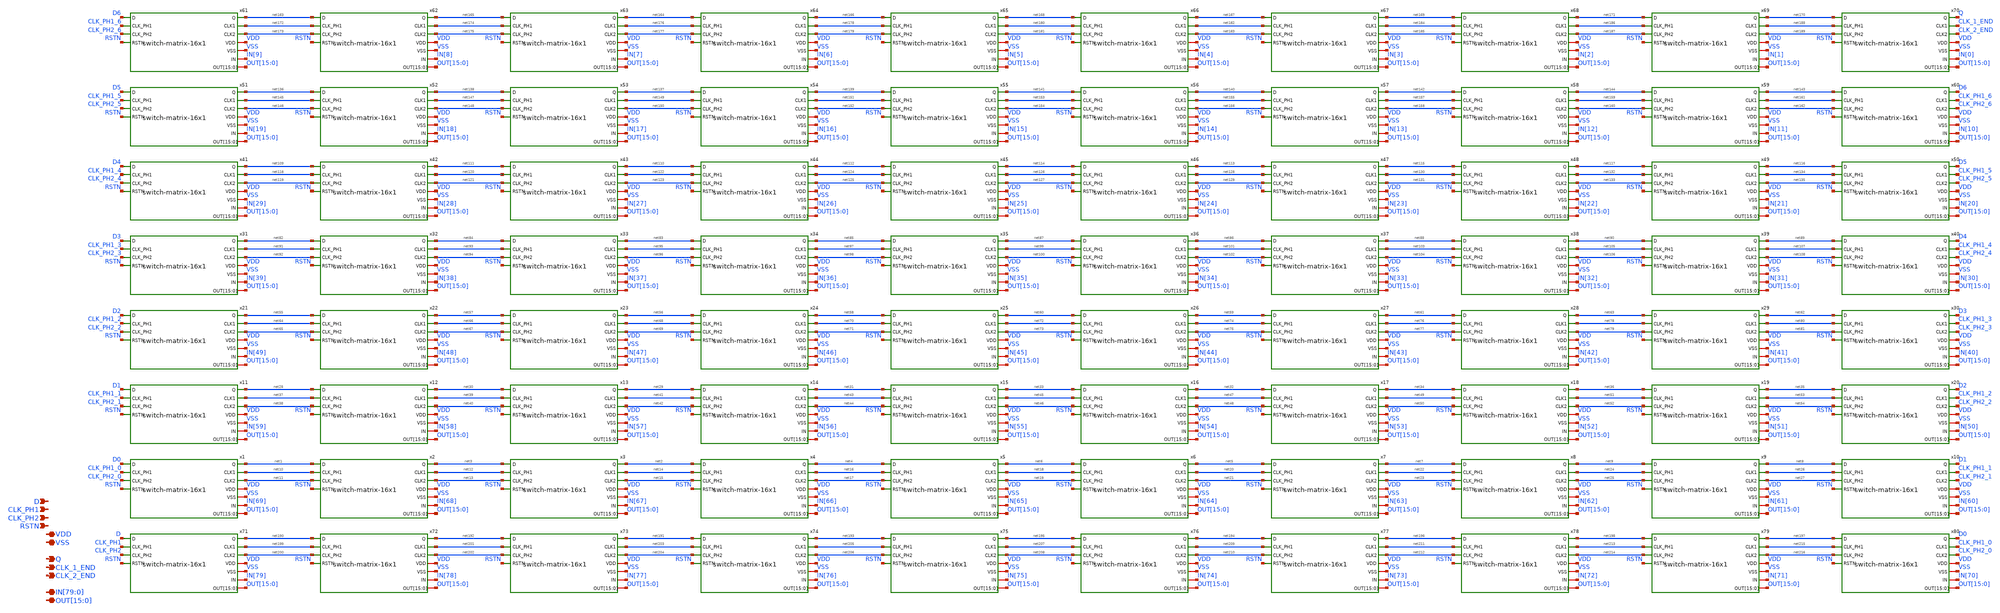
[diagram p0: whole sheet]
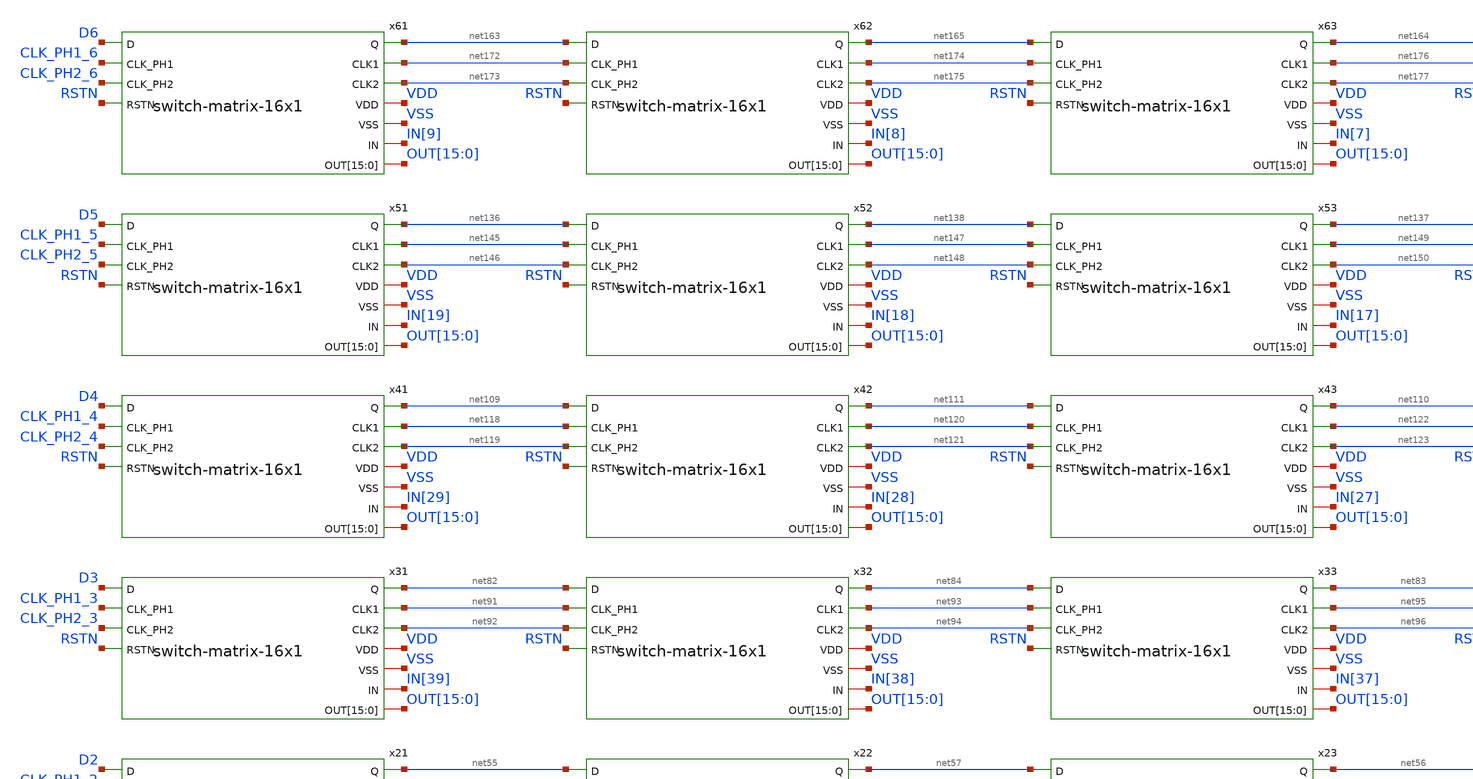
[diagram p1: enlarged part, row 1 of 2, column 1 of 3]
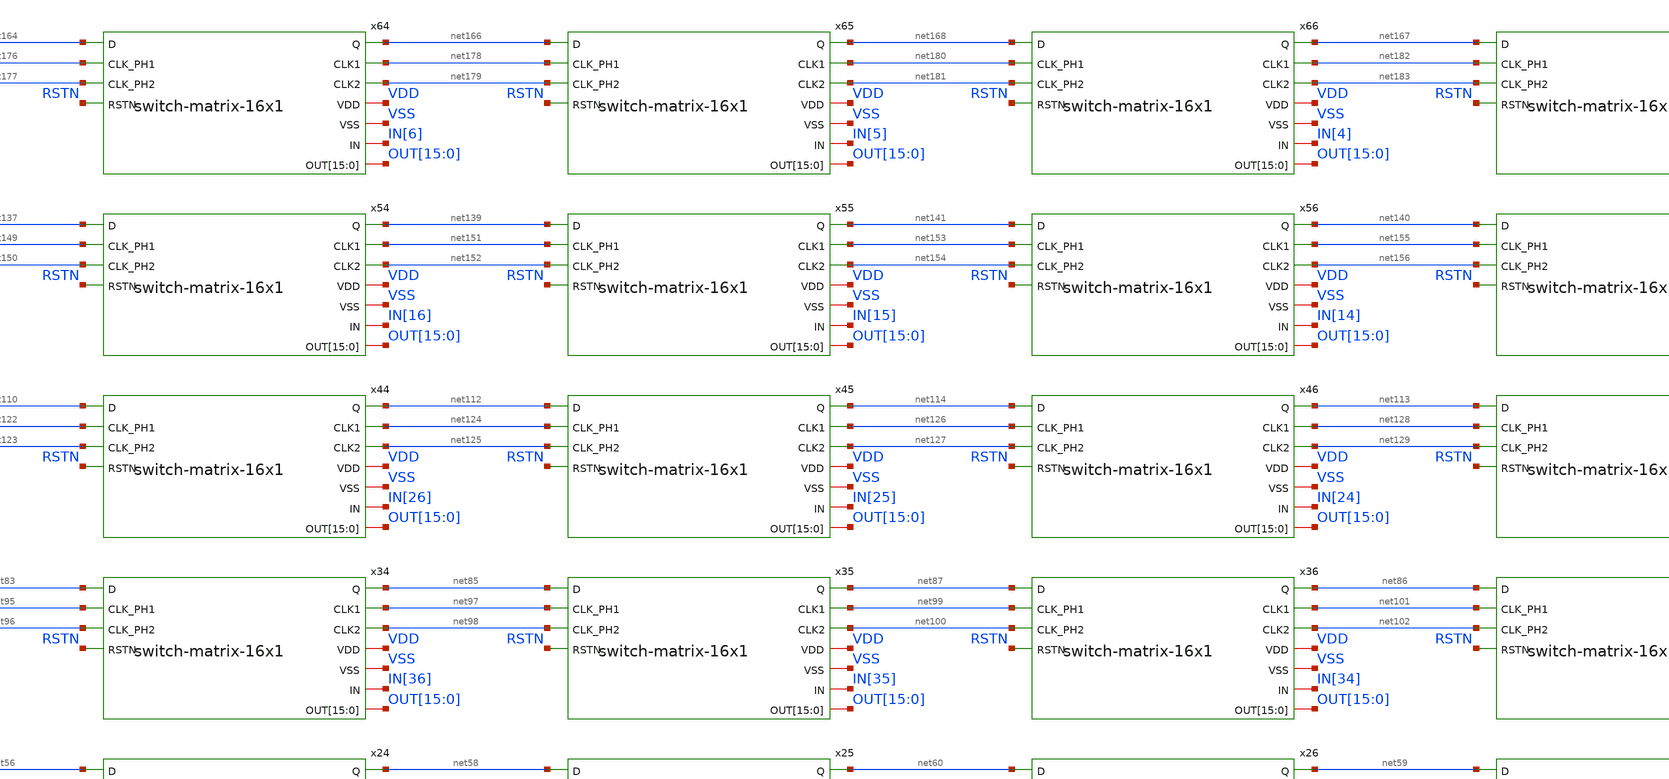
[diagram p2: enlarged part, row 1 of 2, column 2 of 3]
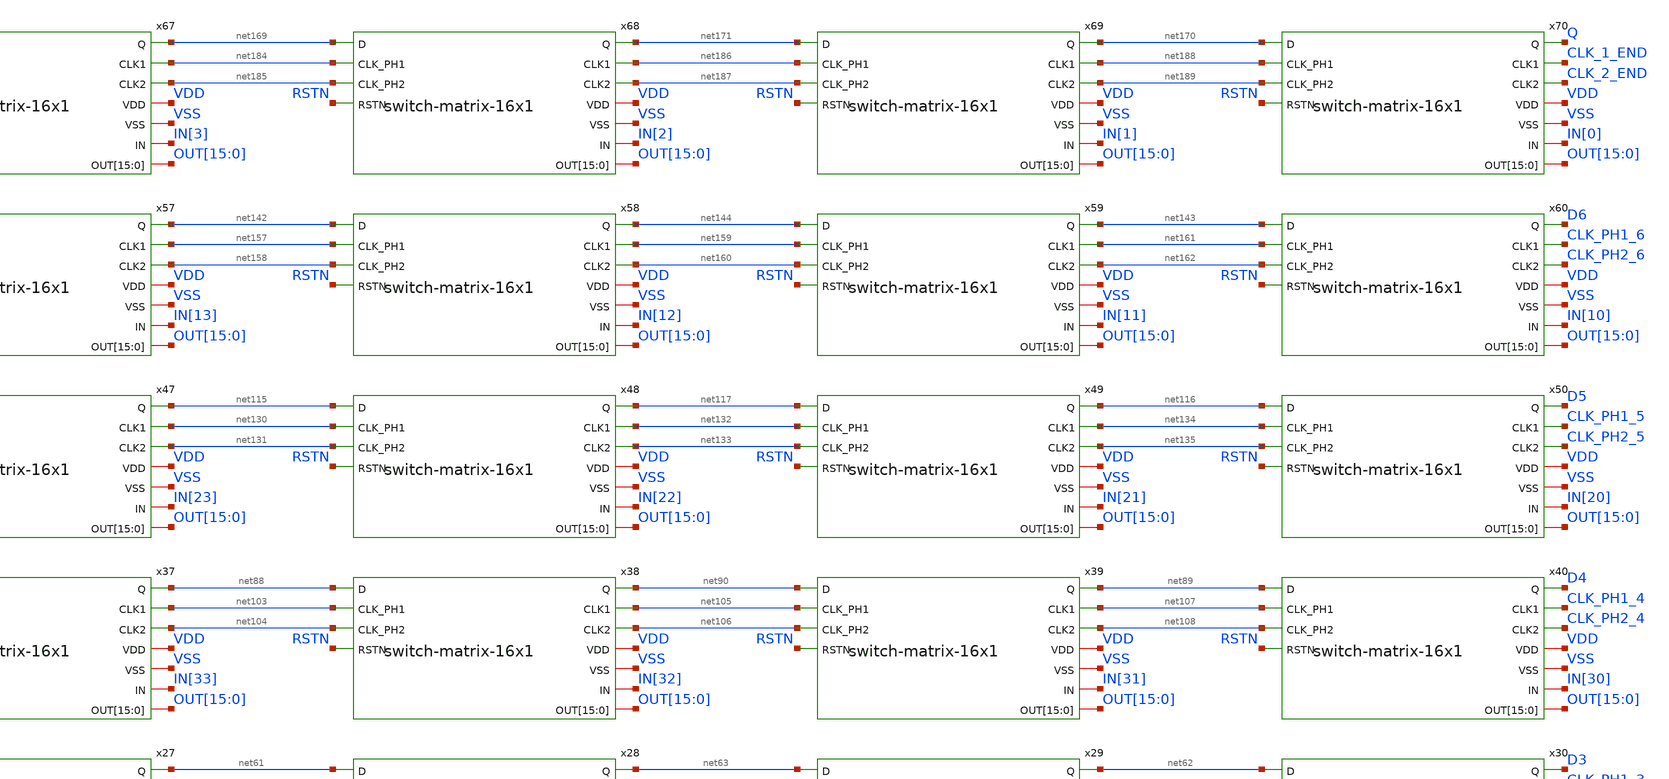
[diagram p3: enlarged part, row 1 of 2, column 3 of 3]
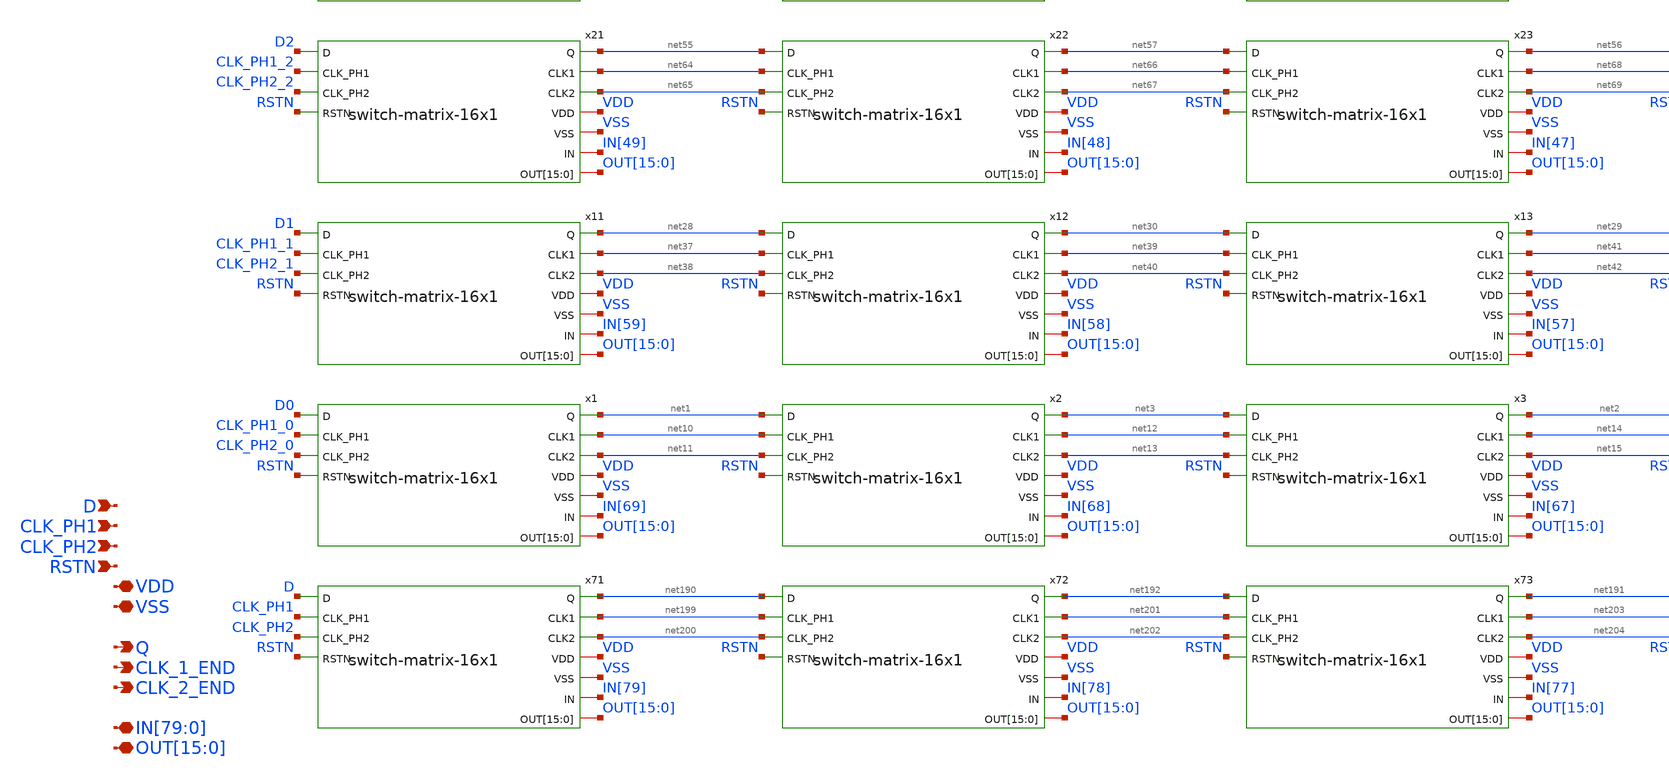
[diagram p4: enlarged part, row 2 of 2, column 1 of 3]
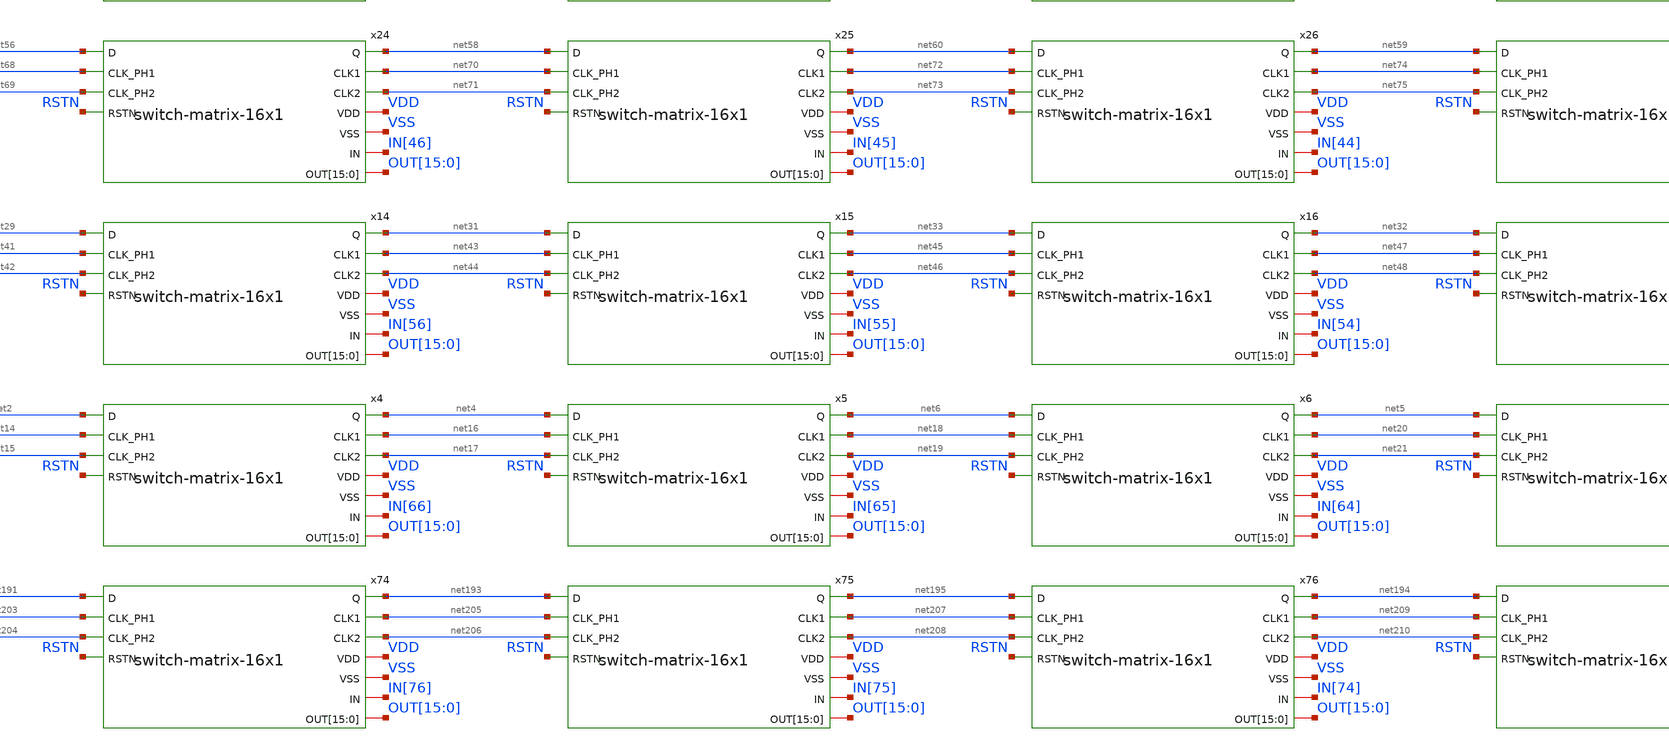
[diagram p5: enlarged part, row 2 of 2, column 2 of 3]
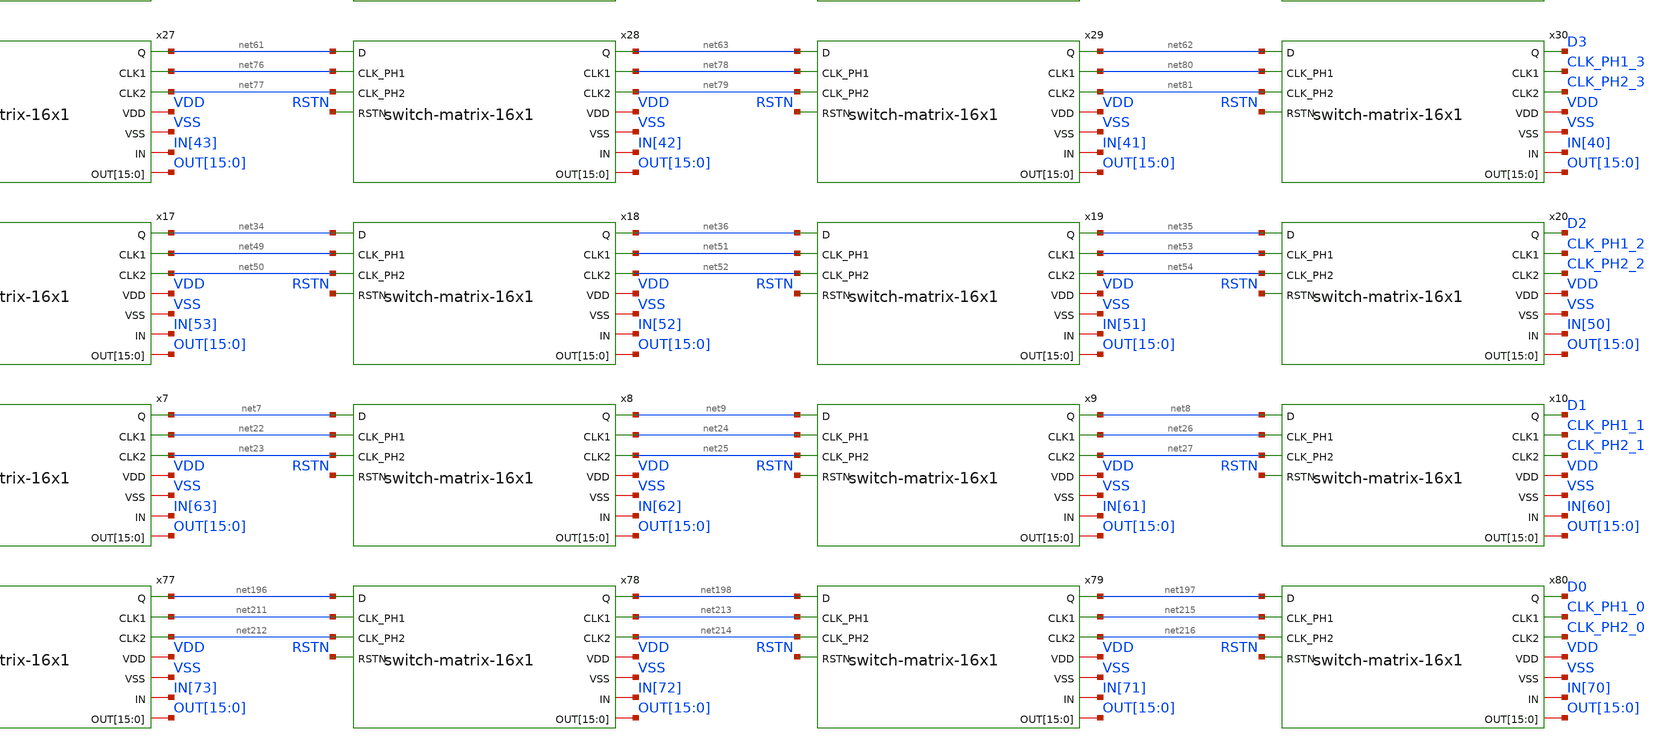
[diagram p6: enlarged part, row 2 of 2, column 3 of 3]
** sch_path: designs/libs/core_switch-matrix/switch-matrix-16x70/switch-matrix-16x70.sch
**.subckt switch-matrix-16x70 VDD VSS RSTN CLK_PH1 CLK_PH2 D
*+ IN[79],IN[78],IN[77],IN[76],IN[75],IN[74],IN[73],IN[72],IN[71],IN[70],IN[69],IN[68],IN[67],IN[66],IN[65],IN[64],IN[63],IN[62],IN[61],IN[60],IN[59],IN[58],IN[57],IN[56],IN[55],IN[54],IN[53],IN[52],IN[51],IN[50],IN[49],IN[48],IN[47],IN[46],IN[45],IN[44],IN[43],IN[42],IN[41],IN[40],IN[39],IN[38],IN[37],IN[36],IN[35],IN[34],IN[33],IN[32],IN[31],IN[30],IN[29],IN[28],IN[27],IN[26],IN[25],IN[24],IN[23],IN[22],IN[21],IN[20],IN[19],IN[18],IN[17],IN[16],IN[15],IN[14],IN[13],IN[12],IN[11],IN[10],IN[9],IN[8],IN[7],IN[6],IN[5],IN[4],IN[3],IN[2],IN[1],IN[0]
*+ OUT[15],OUT[14],OUT[13],OUT[12],OUT[11],OUT[10],OUT[9],OUT[8],OUT[7],OUT[6],OUT[5],OUT[4],OUT[3],OUT[2],OUT[1],OUT[0] Q CLK_1_END CLK_2_END
*.iopin VDD
*.iopin VSS
*.ipin RSTN
*.ipin CLK_PH1
*.ipin CLK_PH2
*.ipin D
*.iopin
*+ IN[79],IN[78],IN[77],IN[76],IN[75],IN[74],IN[73],IN[72],IN[71],IN[70],IN[69],IN[68],IN[67],IN[66],IN[65],IN[64],IN[63],IN[62],IN[61],IN[60],IN[59],IN[58],IN[57],IN[56],IN[55],IN[54],IN[53],IN[52],IN[51],IN[50],IN[49],IN[48],IN[47],IN[46],IN[45],IN[44],IN[43],IN[42],IN[41],IN[40],IN[39],IN[38],IN[37],IN[36],IN[35],IN[34],IN[33],IN[32],IN[31],IN[30],IN[29],IN[28],IN[27],IN[26],IN[25],IN[24],IN[23],IN[22],IN[21],IN[20],IN[19],IN[18],IN[17],IN[16],IN[15],IN[14],IN[13],IN[12],IN[11],IN[10],IN[9],IN[8],IN[7],IN[6],IN[5],IN[4],IN[3],IN[2],IN[1],IN[0]
*.iopin
*+ OUT[15],OUT[14],OUT[13],OUT[12],OUT[11],OUT[10],OUT[9],OUT[8],OUT[7],OUT[6],OUT[5],OUT[4],OUT[3],OUT[2],OUT[1],OUT[0]
*.opin Q
*.opin CLK_1_END
*.opin CLK_2_END
x1 net1 net10 net11 VDD VSS IN[69] OUT[15] OUT[14] OUT[13] OUT[12] OUT[11] OUT[10] OUT[9] OUT[8]
+ OUT[7] OUT[6] OUT[5] OUT[4] OUT[3] OUT[2] OUT[1] OUT[0] D0 CLK_PH1_0 CLK_PH2_0 RSTN switch-matrix-16x1
x2 net3 net12 net13 VDD VSS IN[68] OUT[15] OUT[14] OUT[13] OUT[12] OUT[11] OUT[10] OUT[9] OUT[8]
+ OUT[7] OUT[6] OUT[5] OUT[4] OUT[3] OUT[2] OUT[1] OUT[0] net1 net10 net11 RSTN switch-matrix-16x1
x3 net2 net14 net15 VDD VSS IN[67] OUT[15] OUT[14] OUT[13] OUT[12] OUT[11] OUT[10] OUT[9] OUT[8]
+ OUT[7] OUT[6] OUT[5] OUT[4] OUT[3] OUT[2] OUT[1] OUT[0] net3 net12 net13 RSTN switch-matrix-16x1
x4 net4 net16 net17 VDD VSS IN[66] OUT[15] OUT[14] OUT[13] OUT[12] OUT[11] OUT[10] OUT[9] OUT[8]
+ OUT[7] OUT[6] OUT[5] OUT[4] OUT[3] OUT[2] OUT[1] OUT[0] net2 net14 net15 RSTN switch-matrix-16x1
x5 net6 net18 net19 VDD VSS IN[65] OUT[15] OUT[14] OUT[13] OUT[12] OUT[11] OUT[10] OUT[9] OUT[8]
+ OUT[7] OUT[6] OUT[5] OUT[4] OUT[3] OUT[2] OUT[1] OUT[0] net4 net16 net17 RSTN switch-matrix-16x1
x6 net5 net20 net21 VDD VSS IN[64] OUT[15] OUT[14] OUT[13] OUT[12] OUT[11] OUT[10] OUT[9] OUT[8]
+ OUT[7] OUT[6] OUT[5] OUT[4] OUT[3] OUT[2] OUT[1] OUT[0] net6 net18 net19 RSTN switch-matrix-16x1
x7 net7 net22 net23 VDD VSS IN[63] OUT[15] OUT[14] OUT[13] OUT[12] OUT[11] OUT[10] OUT[9] OUT[8]
+ OUT[7] OUT[6] OUT[5] OUT[4] OUT[3] OUT[2] OUT[1] OUT[0] net5 net20 net21 RSTN switch-matrix-16x1
x8 net9 net24 net25 VDD VSS IN[62] OUT[15] OUT[14] OUT[13] OUT[12] OUT[11] OUT[10] OUT[9] OUT[8]
+ OUT[7] OUT[6] OUT[5] OUT[4] OUT[3] OUT[2] OUT[1] OUT[0] net7 net22 net23 RSTN switch-matrix-16x1
x9 net8 net26 net27 VDD VSS IN[61] OUT[15] OUT[14] OUT[13] OUT[12] OUT[11] OUT[10] OUT[9] OUT[8]
+ OUT[7] OUT[6] OUT[5] OUT[4] OUT[3] OUT[2] OUT[1] OUT[0] net9 net24 net25 RSTN switch-matrix-16x1
x10 D1 CLK_PH1_1 CLK_PH2_1 VDD VSS IN[60] OUT[15] OUT[14] OUT[13] OUT[12] OUT[11] OUT[10] OUT[9]
+ OUT[8] OUT[7] OUT[6] OUT[5] OUT[4] OUT[3] OUT[2] OUT[1] OUT[0] net8 net26 net27 RSTN switch-matrix-16x1
x11 net28 net37 net38 VDD VSS IN[59] OUT[15] OUT[14] OUT[13] OUT[12] OUT[11] OUT[10] OUT[9] OUT[8]
+ OUT[7] OUT[6] OUT[5] OUT[4] OUT[3] OUT[2] OUT[1] OUT[0] D1 CLK_PH1_1 CLK_PH2_1 RSTN switch-matrix-16x1
x12 net30 net39 net40 VDD VSS IN[58] OUT[15] OUT[14] OUT[13] OUT[12] OUT[11] OUT[10] OUT[9] OUT[8]
+ OUT[7] OUT[6] OUT[5] OUT[4] OUT[3] OUT[2] OUT[1] OUT[0] net28 net37 net38 RSTN switch-matrix-16x1
x13 net29 net41 net42 VDD VSS IN[57] OUT[15] OUT[14] OUT[13] OUT[12] OUT[11] OUT[10] OUT[9] OUT[8]
+ OUT[7] OUT[6] OUT[5] OUT[4] OUT[3] OUT[2] OUT[1] OUT[0] net30 net39 net40 RSTN switch-matrix-16x1
x14 net31 net43 net44 VDD VSS IN[56] OUT[15] OUT[14] OUT[13] OUT[12] OUT[11] OUT[10] OUT[9] OUT[8]
+ OUT[7] OUT[6] OUT[5] OUT[4] OUT[3] OUT[2] OUT[1] OUT[0] net29 net41 net42 RSTN switch-matrix-16x1
x15 net33 net45 net46 VDD VSS IN[55] OUT[15] OUT[14] OUT[13] OUT[12] OUT[11] OUT[10] OUT[9] OUT[8]
+ OUT[7] OUT[6] OUT[5] OUT[4] OUT[3] OUT[2] OUT[1] OUT[0] net31 net43 net44 RSTN switch-matrix-16x1
x16 net32 net47 net48 VDD VSS IN[54] OUT[15] OUT[14] OUT[13] OUT[12] OUT[11] OUT[10] OUT[9] OUT[8]
+ OUT[7] OUT[6] OUT[5] OUT[4] OUT[3] OUT[2] OUT[1] OUT[0] net33 net45 net46 RSTN switch-matrix-16x1
x17 net34 net49 net50 VDD VSS IN[53] OUT[15] OUT[14] OUT[13] OUT[12] OUT[11] OUT[10] OUT[9] OUT[8]
+ OUT[7] OUT[6] OUT[5] OUT[4] OUT[3] OUT[2] OUT[1] OUT[0] net32 net47 net48 RSTN switch-matrix-16x1
x18 net36 net51 net52 VDD VSS IN[52] OUT[15] OUT[14] OUT[13] OUT[12] OUT[11] OUT[10] OUT[9] OUT[8]
+ OUT[7] OUT[6] OUT[5] OUT[4] OUT[3] OUT[2] OUT[1] OUT[0] net34 net49 net50 RSTN switch-matrix-16x1
x19 net35 net53 net54 VDD VSS IN[51] OUT[15] OUT[14] OUT[13] OUT[12] OUT[11] OUT[10] OUT[9] OUT[8]
+ OUT[7] OUT[6] OUT[5] OUT[4] OUT[3] OUT[2] OUT[1] OUT[0] net36 net51 net52 RSTN switch-matrix-16x1
x20 D2 CLK_PH1_2 CLK_PH2_2 VDD VSS IN[50] OUT[15] OUT[14] OUT[13] OUT[12] OUT[11] OUT[10] OUT[9]
+ OUT[8] OUT[7] OUT[6] OUT[5] OUT[4] OUT[3] OUT[2] OUT[1] OUT[0] net35 net53 net54 RSTN switch-matrix-16x1
x21 net55 net64 net65 VDD VSS IN[49] OUT[15] OUT[14] OUT[13] OUT[12] OUT[11] OUT[10] OUT[9] OUT[8]
+ OUT[7] OUT[6] OUT[5] OUT[4] OUT[3] OUT[2] OUT[1] OUT[0] D2 CLK_PH1_2 CLK_PH2_2 RSTN switch-matrix-16x1
x22 net57 net66 net67 VDD VSS IN[48] OUT[15] OUT[14] OUT[13] OUT[12] OUT[11] OUT[10] OUT[9] OUT[8]
+ OUT[7] OUT[6] OUT[5] OUT[4] OUT[3] OUT[2] OUT[1] OUT[0] net55 net64 net65 RSTN switch-matrix-16x1
x23 net56 net68 net69 VDD VSS IN[47] OUT[15] OUT[14] OUT[13] OUT[12] OUT[11] OUT[10] OUT[9] OUT[8]
+ OUT[7] OUT[6] OUT[5] OUT[4] OUT[3] OUT[2] OUT[1] OUT[0] net57 net66 net67 RSTN switch-matrix-16x1
x24 net58 net70 net71 VDD VSS IN[46] OUT[15] OUT[14] OUT[13] OUT[12] OUT[11] OUT[10] OUT[9] OUT[8]
+ OUT[7] OUT[6] OUT[5] OUT[4] OUT[3] OUT[2] OUT[1] OUT[0] net56 net68 net69 RSTN switch-matrix-16x1
x25 net60 net72 net73 VDD VSS IN[45] OUT[15] OUT[14] OUT[13] OUT[12] OUT[11] OUT[10] OUT[9] OUT[8]
+ OUT[7] OUT[6] OUT[5] OUT[4] OUT[3] OUT[2] OUT[1] OUT[0] net58 net70 net71 RSTN switch-matrix-16x1
x26 net59 net74 net75 VDD VSS IN[44] OUT[15] OUT[14] OUT[13] OUT[12] OUT[11] OUT[10] OUT[9] OUT[8]
+ OUT[7] OUT[6] OUT[5] OUT[4] OUT[3] OUT[2] OUT[1] OUT[0] net60 net72 net73 RSTN switch-matrix-16x1
x27 net61 net76 net77 VDD VSS IN[43] OUT[15] OUT[14] OUT[13] OUT[12] OUT[11] OUT[10] OUT[9] OUT[8]
+ OUT[7] OUT[6] OUT[5] OUT[4] OUT[3] OUT[2] OUT[1] OUT[0] net59 net74 net75 RSTN switch-matrix-16x1
x28 net63 net78 net79 VDD VSS IN[42] OUT[15] OUT[14] OUT[13] OUT[12] OUT[11] OUT[10] OUT[9] OUT[8]
+ OUT[7] OUT[6] OUT[5] OUT[4] OUT[3] OUT[2] OUT[1] OUT[0] net61 net76 net77 RSTN switch-matrix-16x1
x29 net62 net80 net81 VDD VSS IN[41] OUT[15] OUT[14] OUT[13] OUT[12] OUT[11] OUT[10] OUT[9] OUT[8]
+ OUT[7] OUT[6] OUT[5] OUT[4] OUT[3] OUT[2] OUT[1] OUT[0] net63 net78 net79 RSTN switch-matrix-16x1
x30 D3 CLK_PH1_3 CLK_PH2_3 VDD VSS IN[40] OUT[15] OUT[14] OUT[13] OUT[12] OUT[11] OUT[10] OUT[9]
+ OUT[8] OUT[7] OUT[6] OUT[5] OUT[4] OUT[3] OUT[2] OUT[1] OUT[0] net62 net80 net81 RSTN switch-matrix-16x1
x31 net82 net91 net92 VDD VSS IN[39] OUT[15] OUT[14] OUT[13] OUT[12] OUT[11] OUT[10] OUT[9] OUT[8]
+ OUT[7] OUT[6] OUT[5] OUT[4] OUT[3] OUT[2] OUT[1] OUT[0] D3 CLK_PH1_3 CLK_PH2_3 RSTN switch-matrix-16x1
x32 net84 net93 net94 VDD VSS IN[38] OUT[15] OUT[14] OUT[13] OUT[12] OUT[11] OUT[10] OUT[9] OUT[8]
+ OUT[7] OUT[6] OUT[5] OUT[4] OUT[3] OUT[2] OUT[1] OUT[0] net82 net91 net92 RSTN switch-matrix-16x1
x33 net83 net95 net96 VDD VSS IN[37] OUT[15] OUT[14] OUT[13] OUT[12] OUT[11] OUT[10] OUT[9] OUT[8]
+ OUT[7] OUT[6] OUT[5] OUT[4] OUT[3] OUT[2] OUT[1] OUT[0] net84 net93 net94 RSTN switch-matrix-16x1
x34 net85 net97 net98 VDD VSS IN[36] OUT[15] OUT[14] OUT[13] OUT[12] OUT[11] OUT[10] OUT[9] OUT[8]
+ OUT[7] OUT[6] OUT[5] OUT[4] OUT[3] OUT[2] OUT[1] OUT[0] net83 net95 net96 RSTN switch-matrix-16x1
x35 net87 net99 net100 VDD VSS IN[35] OUT[15] OUT[14] OUT[13] OUT[12] OUT[11] OUT[10] OUT[9] OUT[8]
+ OUT[7] OUT[6] OUT[5] OUT[4] OUT[3] OUT[2] OUT[1] OUT[0] net85 net97 net98 RSTN switch-matrix-16x1
x36 net86 net101 net102 VDD VSS IN[34] OUT[15] OUT[14] OUT[13] OUT[12] OUT[11] OUT[10] OUT[9] OUT[8]
+ OUT[7] OUT[6] OUT[5] OUT[4] OUT[3] OUT[2] OUT[1] OUT[0] net87 net99 net100 RSTN switch-matrix-16x1
x37 net88 net103 net104 VDD VSS IN[33] OUT[15] OUT[14] OUT[13] OUT[12] OUT[11] OUT[10] OUT[9] OUT[8]
+ OUT[7] OUT[6] OUT[5] OUT[4] OUT[3] OUT[2] OUT[1] OUT[0] net86 net101 net102 RSTN switch-matrix-16x1
x38 net90 net105 net106 VDD VSS IN[32] OUT[15] OUT[14] OUT[13] OUT[12] OUT[11] OUT[10] OUT[9] OUT[8]
+ OUT[7] OUT[6] OUT[5] OUT[4] OUT[3] OUT[2] OUT[1] OUT[0] net88 net103 net104 RSTN switch-matrix-16x1
x39 net89 net107 net108 VDD VSS IN[31] OUT[15] OUT[14] OUT[13] OUT[12] OUT[11] OUT[10] OUT[9] OUT[8]
+ OUT[7] OUT[6] OUT[5] OUT[4] OUT[3] OUT[2] OUT[1] OUT[0] net90 net105 net106 RSTN switch-matrix-16x1
x40 D4 CLK_PH1_4 CLK_PH2_4 VDD VSS IN[30] OUT[15] OUT[14] OUT[13] OUT[12] OUT[11] OUT[10] OUT[9]
+ OUT[8] OUT[7] OUT[6] OUT[5] OUT[4] OUT[3] OUT[2] OUT[1] OUT[0] net89 net107 net108 RSTN switch-matrix-16x1
x41 net109 net118 net119 VDD VSS IN[29] OUT[15] OUT[14] OUT[13] OUT[12] OUT[11] OUT[10] OUT[9]
+ OUT[8] OUT[7] OUT[6] OUT[5] OUT[4] OUT[3] OUT[2] OUT[1] OUT[0] D4 CLK_PH1_4 CLK_PH2_4 RSTN
+ switch-matrix-16x1
x42 net111 net120 net121 VDD VSS IN[28] OUT[15] OUT[14] OUT[13] OUT[12] OUT[11] OUT[10] OUT[9]
+ OUT[8] OUT[7] OUT[6] OUT[5] OUT[4] OUT[3] OUT[2] OUT[1] OUT[0] net109 net118 net119 RSTN
+ switch-matrix-16x1
x43 net110 net122 net123 VDD VSS IN[27] OUT[15] OUT[14] OUT[13] OUT[12] OUT[11] OUT[10] OUT[9]
+ OUT[8] OUT[7] OUT[6] OUT[5] OUT[4] OUT[3] OUT[2] OUT[1] OUT[0] net111 net120 net121 RSTN
+ switch-matrix-16x1
x44 net112 net124 net125 VDD VSS IN[26] OUT[15] OUT[14] OUT[13] OUT[12] OUT[11] OUT[10] OUT[9]
+ OUT[8] OUT[7] OUT[6] OUT[5] OUT[4] OUT[3] OUT[2] OUT[1] OUT[0] net110 net122 net123 RSTN
+ switch-matrix-16x1
x45 net114 net126 net127 VDD VSS IN[25] OUT[15] OUT[14] OUT[13] OUT[12] OUT[11] OUT[10] OUT[9]
+ OUT[8] OUT[7] OUT[6] OUT[5] OUT[4] OUT[3] OUT[2] OUT[1] OUT[0] net112 net124 net125 RSTN
+ switch-matrix-16x1
x46 net113 net128 net129 VDD VSS IN[24] OUT[15] OUT[14] OUT[13] OUT[12] OUT[11] OUT[10] OUT[9]
+ OUT[8] OUT[7] OUT[6] OUT[5] OUT[4] OUT[3] OUT[2] OUT[1] OUT[0] net114 net126 net127 RSTN
+ switch-matrix-16x1
x47 net115 net130 net131 VDD VSS IN[23] OUT[15] OUT[14] OUT[13] OUT[12] OUT[11] OUT[10] OUT[9]
+ OUT[8] OUT[7] OUT[6] OUT[5] OUT[4] OUT[3] OUT[2] OUT[1] OUT[0] net113 net128 net129 RSTN
+ switch-matrix-16x1
x48 net117 net132 net133 VDD VSS IN[22] OUT[15] OUT[14] OUT[13] OUT[12] OUT[11] OUT[10] OUT[9]
+ OUT[8] OUT[7] OUT[6] OUT[5] OUT[4] OUT[3] OUT[2] OUT[1] OUT[0] net115 net130 net131 RSTN
+ switch-matrix-16x1
x49 net116 net134 net135 VDD VSS IN[21] OUT[15] OUT[14] OUT[13] OUT[12] OUT[11] OUT[10] OUT[9]
+ OUT[8] OUT[7] OUT[6] OUT[5] OUT[4] OUT[3] OUT[2] OUT[1] OUT[0] net117 net132 net133 RSTN
+ switch-matrix-16x1
x50 D5 CLK_PH1_5 CLK_PH2_5 VDD VSS IN[20] OUT[15] OUT[14] OUT[13] OUT[12] OUT[11] OUT[10] OUT[9]
+ OUT[8] OUT[7] OUT[6] OUT[5] OUT[4] OUT[3] OUT[2] OUT[1] OUT[0] net116 net134 net135 RSTN
+ switch-matrix-16x1
x51 net136 net145 net146 VDD VSS IN[19] OUT[15] OUT[14] OUT[13] OUT[12] OUT[11] OUT[10] OUT[9]
+ OUT[8] OUT[7] OUT[6] OUT[5] OUT[4] OUT[3] OUT[2] OUT[1] OUT[0] D5 CLK_PH1_5 CLK_PH2_5 RSTN
+ switch-matrix-16x1
x52 net138 net147 net148 VDD VSS IN[18] OUT[15] OUT[14] OUT[13] OUT[12] OUT[11] OUT[10] OUT[9]
+ OUT[8] OUT[7] OUT[6] OUT[5] OUT[4] OUT[3] OUT[2] OUT[1] OUT[0] net136 net145 net146 RSTN
+ switch-matrix-16x1
x53 net137 net149 net150 VDD VSS IN[17] OUT[15] OUT[14] OUT[13] OUT[12] OUT[11] OUT[10] OUT[9]
+ OUT[8] OUT[7] OUT[6] OUT[5] OUT[4] OUT[3] OUT[2] OUT[1] OUT[0] net138 net147 net148 RSTN
+ switch-matrix-16x1
x54 net139 net151 net152 VDD VSS IN[16] OUT[15] OUT[14] OUT[13] OUT[12] OUT[11] OUT[10] OUT[9]
+ OUT[8] OUT[7] OUT[6] OUT[5] OUT[4] OUT[3] OUT[2] OUT[1] OUT[0] net137 net149 net150 RSTN
+ switch-matrix-16x1
x55 net141 net153 net154 VDD VSS IN[15] OUT[15] OUT[14] OUT[13] OUT[12] OUT[11] OUT[10] OUT[9]
+ OUT[8] OUT[7] OUT[6] OUT[5] OUT[4] OUT[3] OUT[2] OUT[1] OUT[0] net139 net151 net152 RSTN
+ switch-matrix-16x1
x56 net140 net155 net156 VDD VSS IN[14] OUT[15] OUT[14] OUT[13] OUT[12] OUT[11] OUT[10] OUT[9]
+ OUT[8] OUT[7] OUT[6] OUT[5] OUT[4] OUT[3] OUT[2] OUT[1] OUT[0] net141 net153 net154 RSTN
+ switch-matrix-16x1
x57 net142 net157 net158 VDD VSS IN[13] OUT[15] OUT[14] OUT[13] OUT[12] OUT[11] OUT[10] OUT[9]
+ OUT[8] OUT[7] OUT[6] OUT[5] OUT[4] OUT[3] OUT[2] OUT[1] OUT[0] net140 net155 net156 RSTN
+ switch-matrix-16x1
x58 net144 net159 net160 VDD VSS IN[12] OUT[15] OUT[14] OUT[13] OUT[12] OUT[11] OUT[10] OUT[9]
+ OUT[8] OUT[7] OUT[6] OUT[5] OUT[4] OUT[3] OUT[2] OUT[1] OUT[0] net142 net157 net158 RSTN
+ switch-matrix-16x1
x59 net143 net161 net162 VDD VSS IN[11] OUT[15] OUT[14] OUT[13] OUT[12] OUT[11] OUT[10] OUT[9]
+ OUT[8] OUT[7] OUT[6] OUT[5] OUT[4] OUT[3] OUT[2] OUT[1] OUT[0] net144 net159 net160 RSTN
+ switch-matrix-16x1
x60 D6 CLK_PH1_6 CLK_PH2_6 VDD VSS IN[10] OUT[15] OUT[14] OUT[13] OUT[12] OUT[11] OUT[10] OUT[9]
+ OUT[8] OUT[7] OUT[6] OUT[5] OUT[4] OUT[3] OUT[2] OUT[1] OUT[0] net143 net161 net162 RSTN
+ switch-matrix-16x1
x61 net163 net172 net173 VDD VSS IN[9] OUT[15] OUT[14] OUT[13] OUT[12] OUT[11] OUT[10] OUT[9] OUT[8]
+ OUT[7] OUT[6] OUT[5] OUT[4] OUT[3] OUT[2] OUT[1] OUT[0] D6 CLK_PH1_6 CLK_PH2_6 RSTN switch-matrix-16x1
x62 net165 net174 net175 VDD VSS IN[8] OUT[15] OUT[14] OUT[13] OUT[12] OUT[11] OUT[10] OUT[9] OUT[8]
+ OUT[7] OUT[6] OUT[5] OUT[4] OUT[3] OUT[2] OUT[1] OUT[0] net163 net172 net173 RSTN switch-matrix-16x1
x63 net164 net176 net177 VDD VSS IN[7] OUT[15] OUT[14] OUT[13] OUT[12] OUT[11] OUT[10] OUT[9] OUT[8]
+ OUT[7] OUT[6] OUT[5] OUT[4] OUT[3] OUT[2] OUT[1] OUT[0] net165 net174 net175 RSTN switch-matrix-16x1
x64 net166 net178 net179 VDD VSS IN[6] OUT[15] OUT[14] OUT[13] OUT[12] OUT[11] OUT[10] OUT[9] OUT[8]
+ OUT[7] OUT[6] OUT[5] OUT[4] OUT[3] OUT[2] OUT[1] OUT[0] net164 net176 net177 RSTN switch-matrix-16x1
x65 net168 net180 net181 VDD VSS IN[5] OUT[15] OUT[14] OUT[13] OUT[12] OUT[11] OUT[10] OUT[9] OUT[8]
+ OUT[7] OUT[6] OUT[5] OUT[4] OUT[3] OUT[2] OUT[1] OUT[0] net166 net178 net179 RSTN switch-matrix-16x1
x66 net167 net182 net183 VDD VSS IN[4] OUT[15] OUT[14] OUT[13] OUT[12] OUT[11] OUT[10] OUT[9] OUT[8]
+ OUT[7] OUT[6] OUT[5] OUT[4] OUT[3] OUT[2] OUT[1] OUT[0] net168 net180 net181 RSTN switch-matrix-16x1
x67 net169 net184 net185 VDD VSS IN[3] OUT[15] OUT[14] OUT[13] OUT[12] OUT[11] OUT[10] OUT[9] OUT[8]
+ OUT[7] OUT[6] OUT[5] OUT[4] OUT[3] OUT[2] OUT[1] OUT[0] net167 net182 net183 RSTN switch-matrix-16x1
x68 net171 net186 net187 VDD VSS IN[2] OUT[15] OUT[14] OUT[13] OUT[12] OUT[11] OUT[10] OUT[9] OUT[8]
+ OUT[7] OUT[6] OUT[5] OUT[4] OUT[3] OUT[2] OUT[1] OUT[0] net169 net184 net185 RSTN switch-matrix-16x1
x69 net170 net188 net189 VDD VSS IN[1] OUT[15] OUT[14] OUT[13] OUT[12] OUT[11] OUT[10] OUT[9] OUT[8]
+ OUT[7] OUT[6] OUT[5] OUT[4] OUT[3] OUT[2] OUT[1] OUT[0] net171 net186 net187 RSTN switch-matrix-16x1
x70 Q CLK_1_END CLK_2_END VDD VSS IN[0] OUT[15] OUT[14] OUT[13] OUT[12] OUT[11] OUT[10] OUT[9]
+ OUT[8] OUT[7] OUT[6] OUT[5] OUT[4] OUT[3] OUT[2] OUT[1] OUT[0] net170 net188 net189 RSTN
+ switch-matrix-16x1
x71 net190 net199 net200 VDD VSS IN[79] OUT[15] OUT[14] OUT[13] OUT[12] OUT[11] OUT[10] OUT[9]
+ OUT[8] OUT[7] OUT[6] OUT[5] OUT[4] OUT[3] OUT[2] OUT[1] OUT[0] D CLK_PH1 CLK_PH2 RSTN switch-matrix-16x1
x72 net192 net201 net202 VDD VSS IN[78] OUT[15] OUT[14] OUT[13] OUT[12] OUT[11] OUT[10] OUT[9]
+ OUT[8] OUT[7] OUT[6] OUT[5] OUT[4] OUT[3] OUT[2] OUT[1] OUT[0] net190 net199 net200 RSTN
+ switch-matrix-16x1
x73 net191 net203 net204 VDD VSS IN[77] OUT[15] OUT[14] OUT[13] OUT[12] OUT[11] OUT[10] OUT[9]
+ OUT[8] OUT[7] OUT[6] OUT[5] OUT[4] OUT[3] OUT[2] OUT[1] OUT[0] net192 net201 net202 RSTN
+ switch-matrix-16x1
x74 net193 net205 net206 VDD VSS IN[76] OUT[15] OUT[14] OUT[13] OUT[12] OUT[11] OUT[10] OUT[9]
+ OUT[8] OUT[7] OUT[6] OUT[5] OUT[4] OUT[3] OUT[2] OUT[1] OUT[0] net191 net203 net204 RSTN
+ switch-matrix-16x1
x75 net195 net207 net208 VDD VSS IN[75] OUT[15] OUT[14] OUT[13] OUT[12] OUT[11] OUT[10] OUT[9]
+ OUT[8] OUT[7] OUT[6] OUT[5] OUT[4] OUT[3] OUT[2] OUT[1] OUT[0] net193 net205 net206 RSTN
+ switch-matrix-16x1
x76 net194 net209 net210 VDD VSS IN[74] OUT[15] OUT[14] OUT[13] OUT[12] OUT[11] OUT[10] OUT[9]
+ OUT[8] OUT[7] OUT[6] OUT[5] OUT[4] OUT[3] OUT[2] OUT[1] OUT[0] net195 net207 net208 RSTN
+ switch-matrix-16x1
x77 net196 net211 net212 VDD VSS IN[73] OUT[15] OUT[14] OUT[13] OUT[12] OUT[11] OUT[10] OUT[9]
+ OUT[8] OUT[7] OUT[6] OUT[5] OUT[4] OUT[3] OUT[2] OUT[1] OUT[0] net194 net209 net210 RSTN
+ switch-matrix-16x1
x78 net198 net213 net214 VDD VSS IN[72] OUT[15] OUT[14] OUT[13] OUT[12] OUT[11] OUT[10] OUT[9]
+ OUT[8] OUT[7] OUT[6] OUT[5] OUT[4] OUT[3] OUT[2] OUT[1] OUT[0] net196 net211 net212 RSTN
+ switch-matrix-16x1
x79 net197 net215 net216 VDD VSS IN[71] OUT[15] OUT[14] OUT[13] OUT[12] OUT[11] OUT[10] OUT[9]
+ OUT[8] OUT[7] OUT[6] OUT[5] OUT[4] OUT[3] OUT[2] OUT[1] OUT[0] net198 net213 net214 RSTN
+ switch-matrix-16x1
x80 D0 CLK_PH1_0 CLK_PH2_0 VDD VSS IN[70] OUT[15] OUT[14] OUT[13] OUT[12] OUT[11] OUT[10] OUT[9]
+ OUT[8] OUT[7] OUT[6] OUT[5] OUT[4] OUT[3] OUT[2] OUT[1] OUT[0] net197 net215 net216 RSTN
+ switch-matrix-16x1
**.ends
.end
